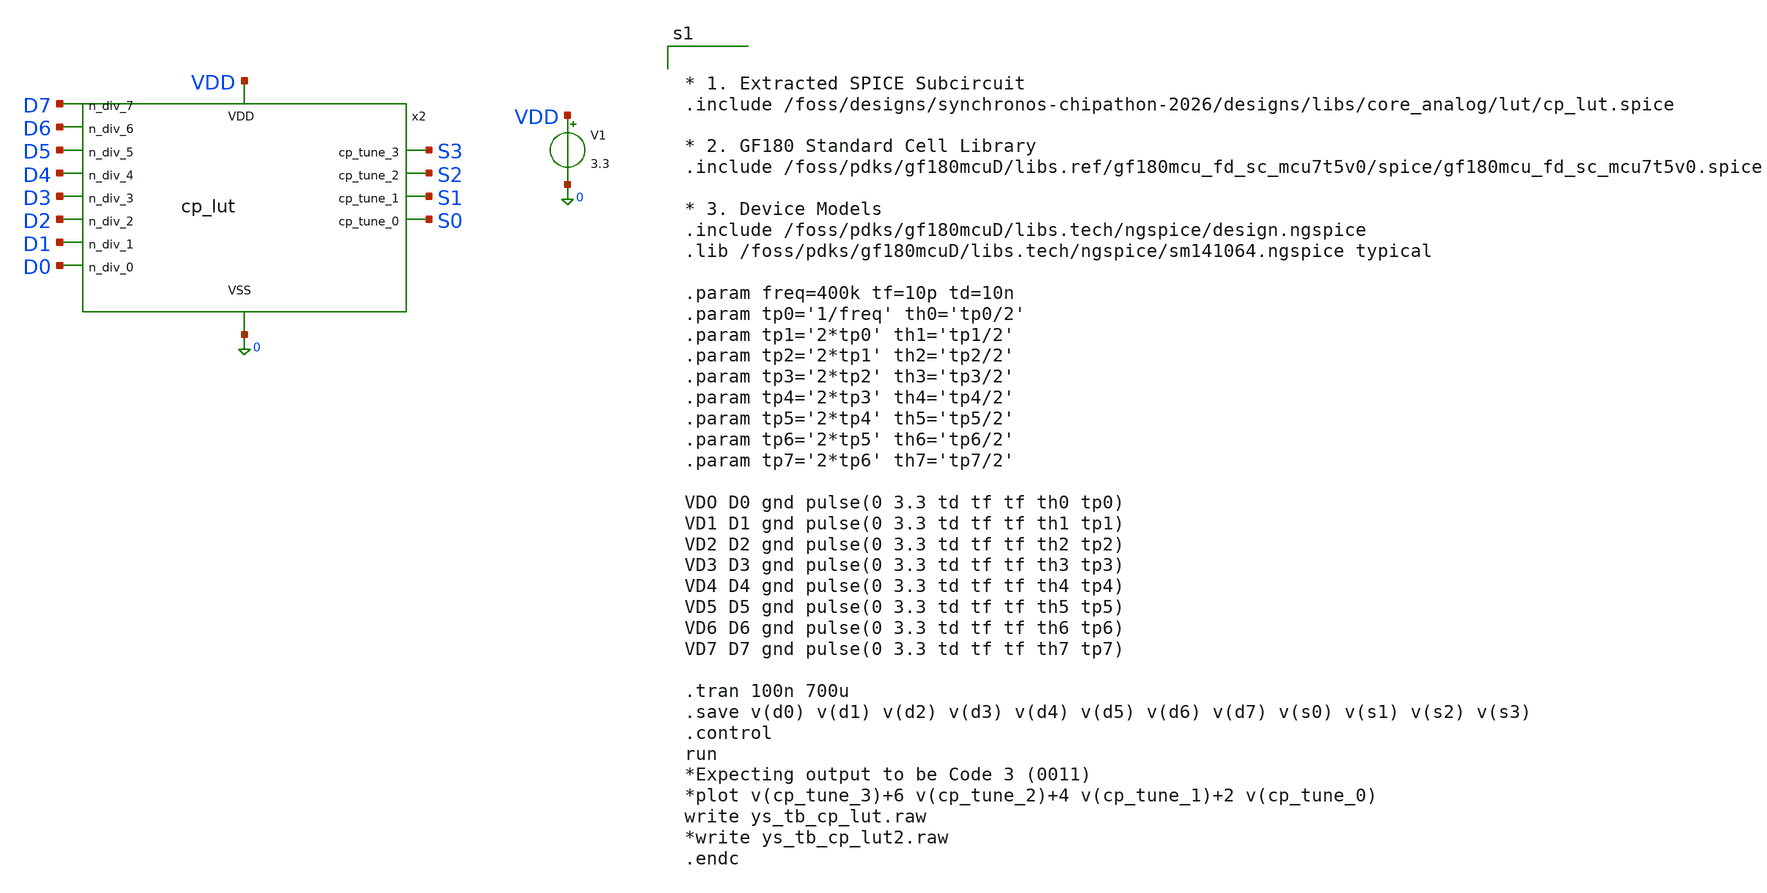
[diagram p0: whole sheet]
** sch_path: designs/libs/tb_analog/tb_lut/ys_tb_cp_lut.sch
**.subckt ys_tb_cp_lut
V1 VDD 0 3.3
x2 VDD 0 S0 S1 S2 S3 D0 D1 D2 D3 D4 D5 D6 D7 cp_lut
**** begin user architecture code


* 1. Extracted SPICE Subcircuit
.include /foss/designs/synchronos-chipathon-2026/designs/libs/core_analog/lut/cp_lut.spice

* 2. GF180 Standard Cell Library
.include /foss/pdks/gf180mcuD/libs.ref/gf180mcu_fd_sc_mcu7t5v0/spice/gf180mcu_fd_sc_mcu7t5v0.spice

* 3. Device Models
.include /foss/pdks/gf180mcuD/libs.tech/ngspice/design.ngspice
.lib /foss/pdks/gf180mcuD/libs.tech/ngspice/sm141064.ngspice typical

.param freq=400k tf=10p td=10n
.param tp0='1/freq' th0='tp0/2'
.param tp1='2*tp0' th1='tp1/2'
.param tp2='2*tp1' th2='tp2/2'
.param tp3='2*tp2' th3='tp3/2'
.param tp4='2*tp3' th4='tp4/2'
.param tp5='2*tp4' th5='tp5/2'
.param tp6='2*tp5' th6='tp6/2'
.param tp7='2*tp6' th7='tp7/2'

VDO D0 gnd pulse(0 3.3 td tf tf th0 tp0)
VD1 D1 gnd pulse(0 3.3 td tf tf th1 tp1)
VD2 D2 gnd pulse(0 3.3 td tf tf th2 tp2)
VD3 D3 gnd pulse(0 3.3 td tf tf th3 tp3)
VD4 D4 gnd pulse(0 3.3 td tf tf th4 tp4)
VD5 D5 gnd pulse(0 3.3 td tf tf th5 tp5)
VD6 D6 gnd pulse(0 3.3 td tf tf th6 tp6)
VD7 D7 gnd pulse(0 3.3 td tf tf th7 tp7)

.tran 100n 700u
.save v(d0) v(d1) v(d2) v(d3) v(d4) v(d5) v(d6) v(d7) v(s0) v(s1) v(s2) v(s3)
.control
run
*Expecting output to be Code 3 (0011)
*plot v(cp_tune_3)+6 v(cp_tune_2)+4 v(cp_tune_1)+2 v(cp_tune_0)
write ys_tb_cp_lut.raw
*write ys_tb_cp_lut2.raw
.endc

**** end user architecture code
**.ends
.end
